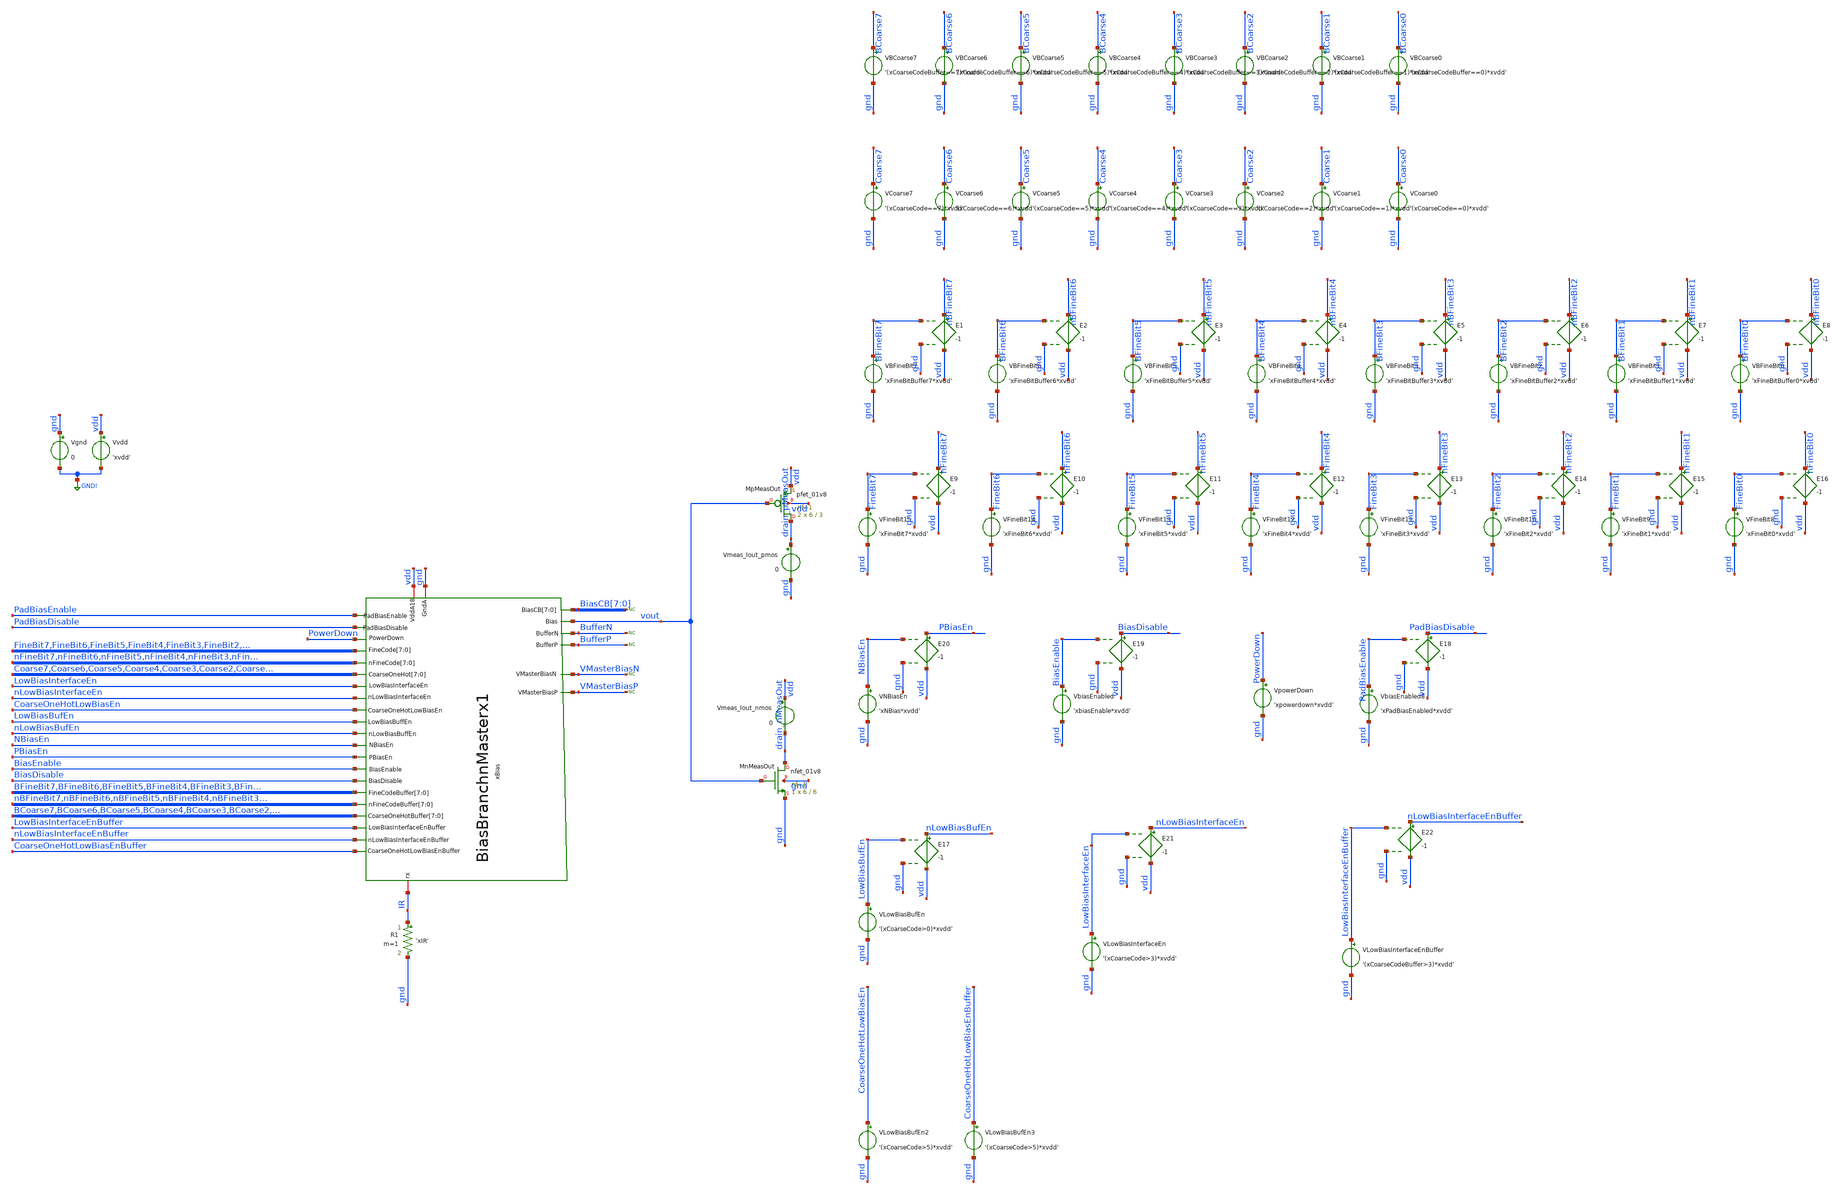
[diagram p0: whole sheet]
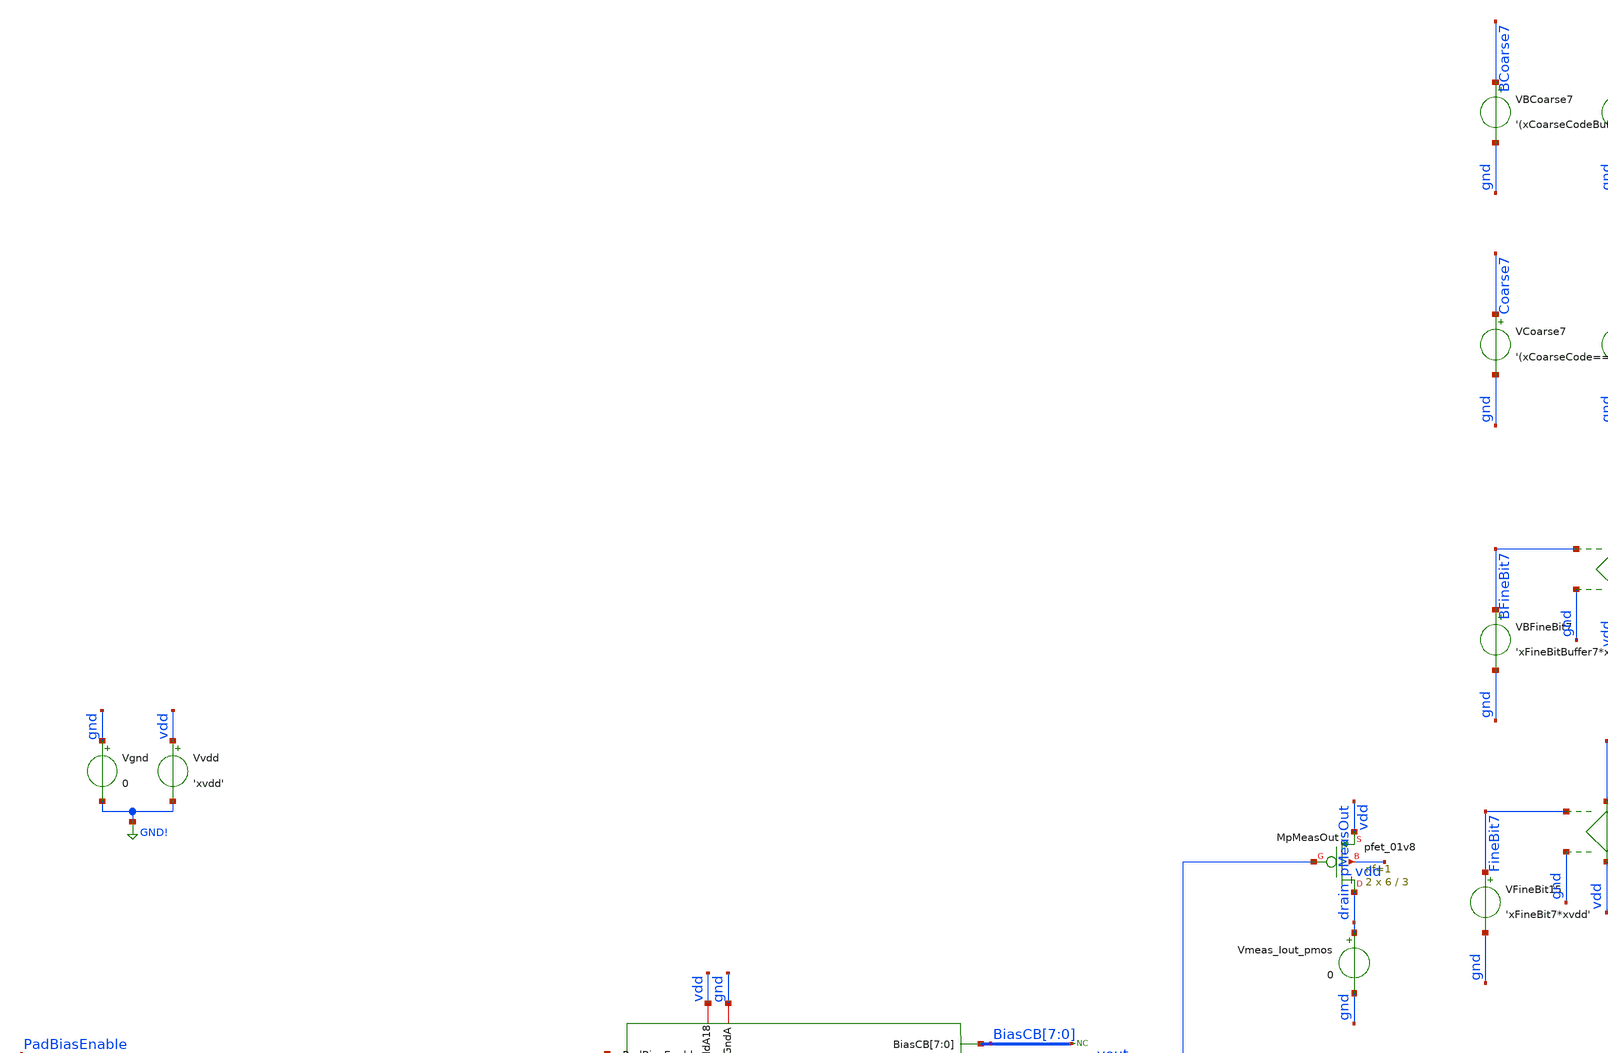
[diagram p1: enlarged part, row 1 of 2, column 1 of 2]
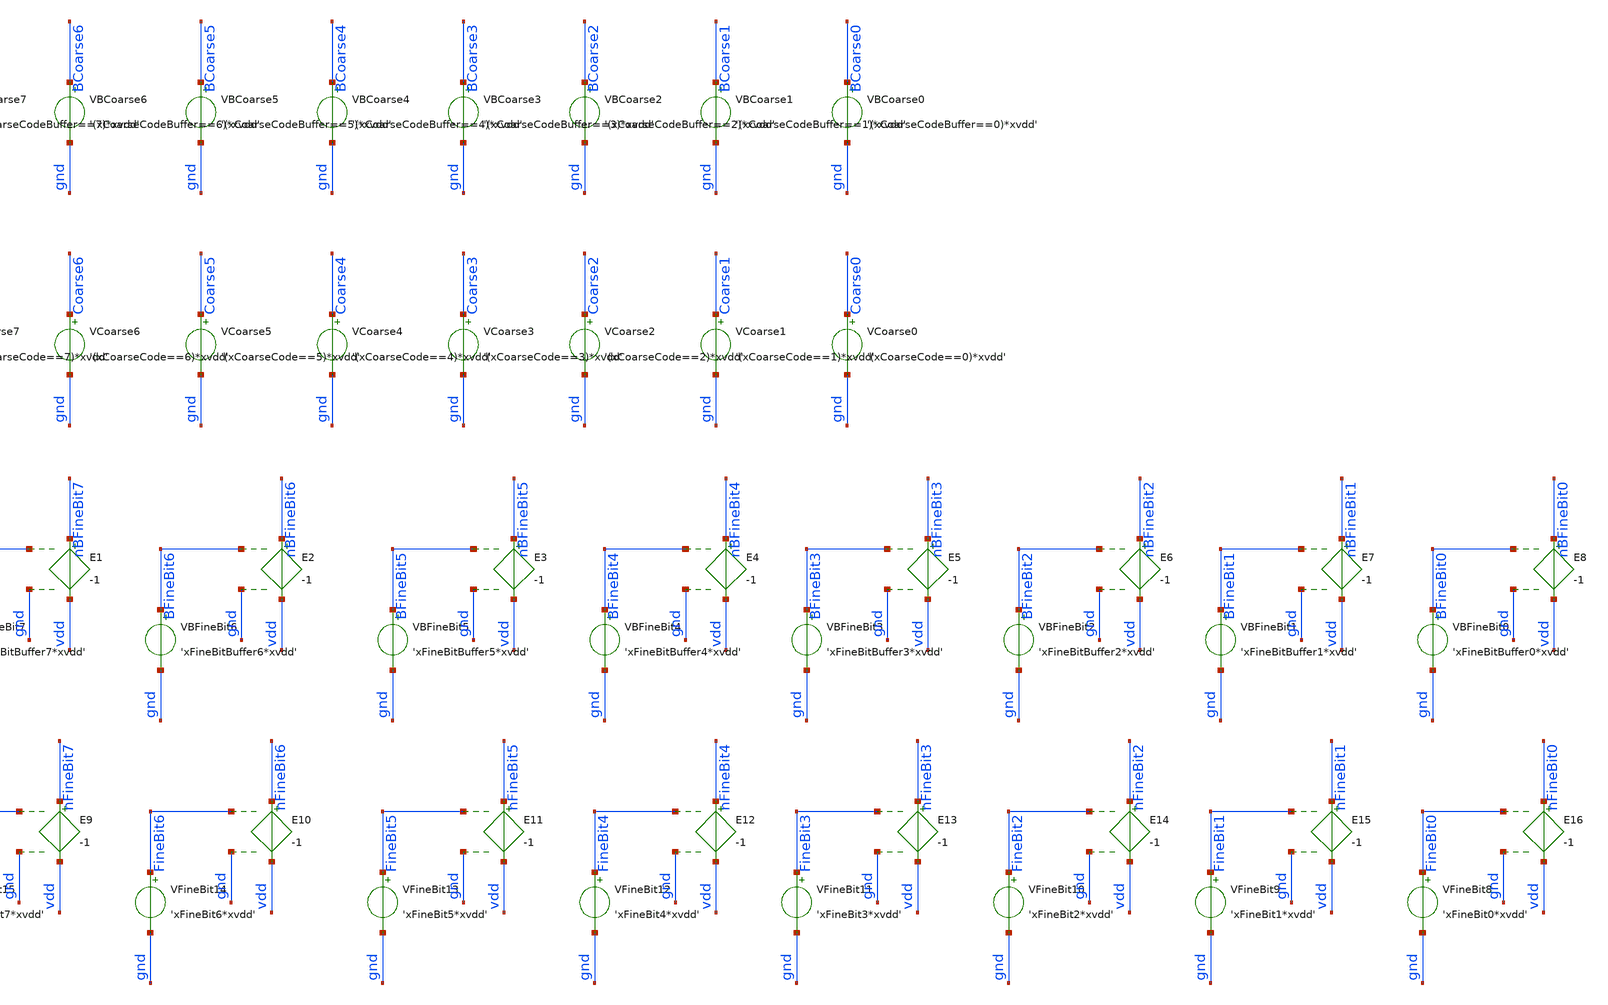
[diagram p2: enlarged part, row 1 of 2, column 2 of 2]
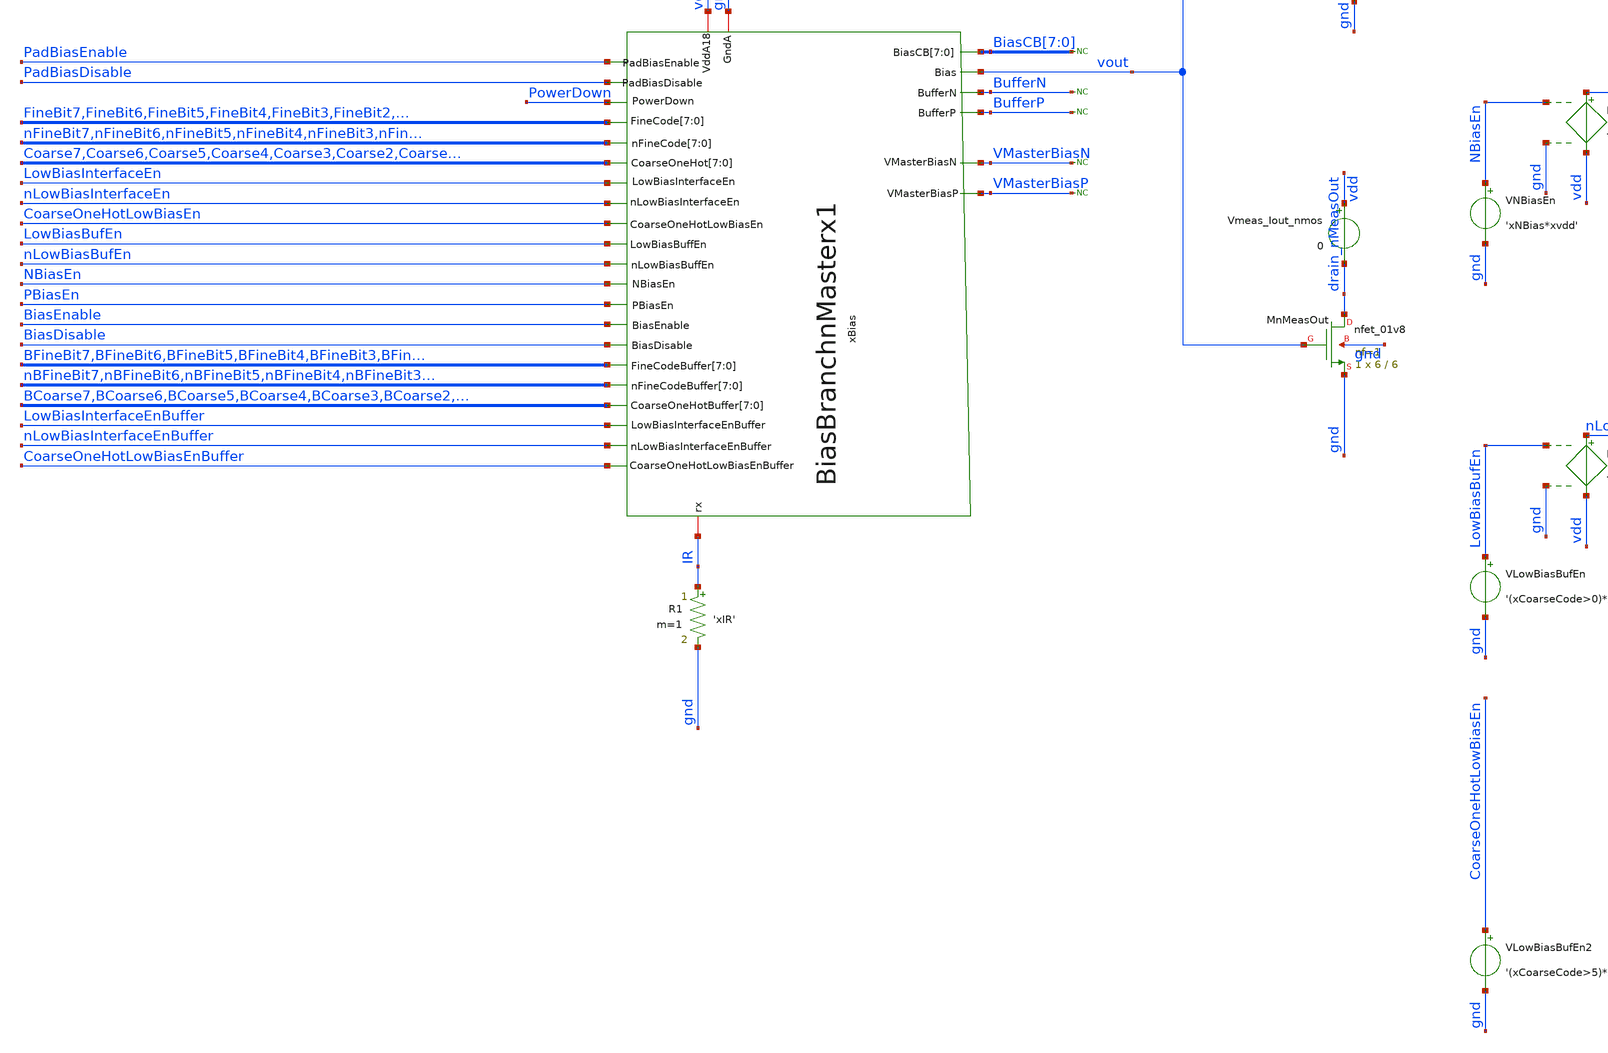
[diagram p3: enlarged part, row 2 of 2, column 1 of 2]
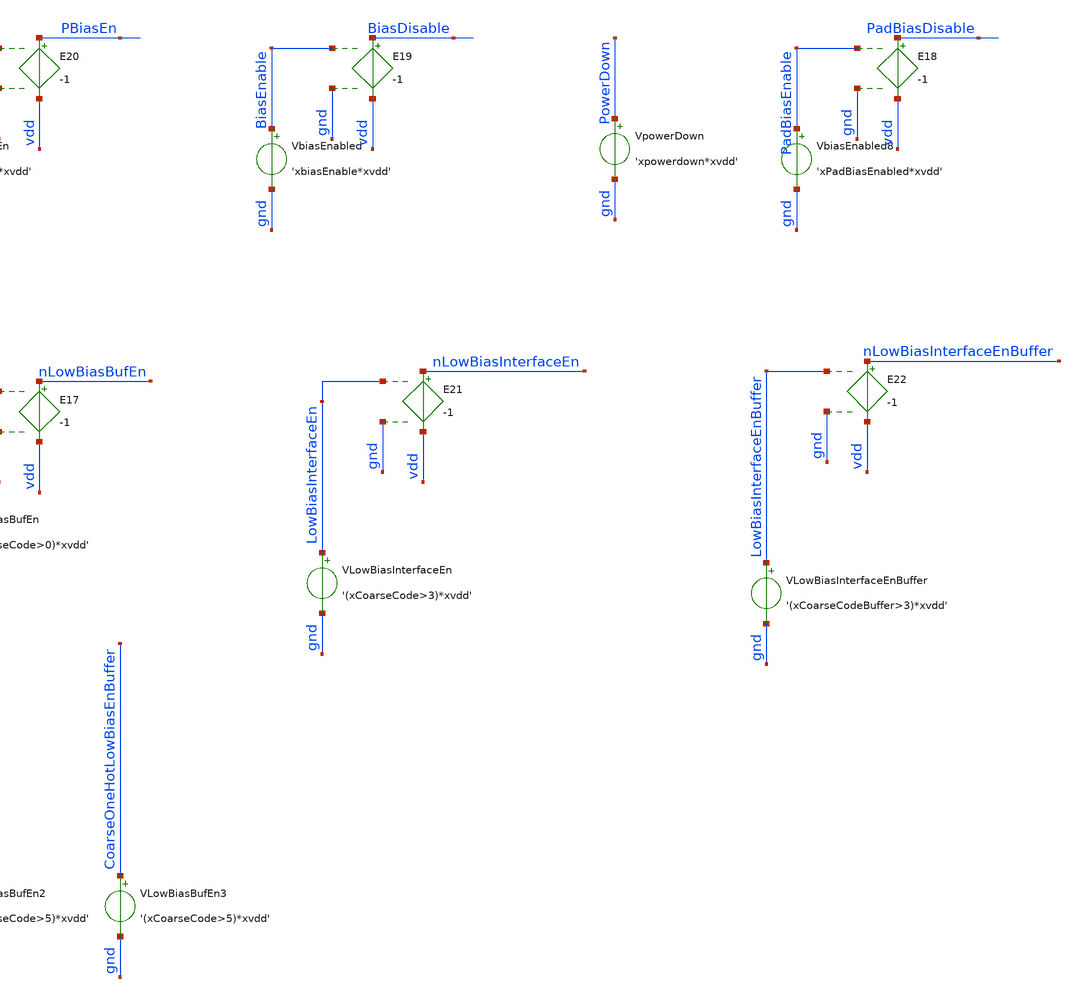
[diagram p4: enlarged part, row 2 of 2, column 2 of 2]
** sch_path: analog/xschem/tb_BiasBranchnMasterx1_op.sch
**.subckt tb_BiasBranchnMasterx1_op
Vgnd gnd GND! 0
.save i(vgnd)
Vvdd vdd GND! 'xvdd'
.save i(vvdd)
VpowerDown PowerDown gnd 'xpowerdown*xvdd'
.save i(vpowerdown)
XMnMeasOut drain_nMeasOut vout gnd gnd sky130_fd_pr__nfet_01v8 L=6 W=6 nf=1 ad='int((1 + 1)/2) * 6 / 1 * 0.29'
+ as='int((1 + 2)/2) * 6 / 1 * 0.29' pd='2*int((1 + 1)/2) * (6 / 1 + 0.29)' ps='2*int((1 + 2)/2) * (6 / 1 + 0.29)'
+ nrd='0.29 / 6 ' nrs='0.29 / 6 ' sa=0 sb=0 sd=0 mult=1 m=1
Vmeas_Iout_nmos vdd drain_nMeasOut 0
.save i(vmeas_iout_nmos)
XMpMeasOut drain_pMeasOut vout vdd vdd sky130_fd_pr__pfet_01v8 L=3 W=6 nf=1 ad='int((1 + 1)/2) * 6 / 1 * 0.29'
+ as='int((1 + 2)/2) * 6 / 1 * 0.29' pd='2*int((1 + 1)/2) * (6 / 1 + 0.29)' ps='2*int((1 + 2)/2) * (6 / 1 + 0.29)'
+ nrd='0.29 / 6 ' nrs='0.29 / 6 ' sa=0 sb=0 sd=0 mult=2 m=2
Vmeas_Iout_pmos drain_pMeasOut gnd 0
.save i(vmeas_iout_pmos)
VbiasEnabled BiasEnable gnd 'xbiasEnable*xvdd'
VNBiasEn NBiasEn gnd 'xNBias*xvdd'
xBias vdd gnd PowerDown BiasCB[7] BiasCB[6] BiasCB[5] BiasCB[4] BiasCB[3] BiasCB[2] BiasCB[1]
+ BiasCB[0] BufferN BufferP VMasterBiasN VMasterBiasP vout IR Coarse7 Coarse6 Coarse5 Coarse4 Coarse3 Coarse2
+ Coarse1 Coarse0 LowBiasInterfaceEn nLowBiasInterfaceEn FineBit7 FineBit6 FineBit5 FineBit4 FineBit3
+ FineBit2 FineBit1 FineBit0 nFineBit7 nFineBit6 nFineBit5 nFineBit4 nFineBit3 nFineBit2 nFineBit1 nFineBit0
+ CoarseOneHotLowBiasEn LowBiasBufEn nLowBiasBufEn NBiasEn PBiasEn BiasEnable BiasDisable BCoarse7 BCoarse6 BCoarse5
+ BCoarse4 BCoarse3 BCoarse2 BCoarse1 BCoarse0 LowBiasInterfaceEnBuffer nLowBiasInterfaceEnBuffer BFineBit7
+ BFineBit6 BFineBit5 BFineBit4 BFineBit3 BFineBit2 BFineBit1 BFineBit0 nBFineBit7 nBFineBit6 nBFineBit5
+ nBFineBit4 nBFineBit3 nBFineBit2 nBFineBit1 nBFineBit0 CoarseOneHotLowBiasEnBuffer PadBiasEnable
+ PadBiasDisable BiasBranchnMasterx1
* noconn BiasCB[7:0]
* noconn BufferN
* noconn BufferP
* noconn VMasterBiasN
* noconn VMasterBiasP
R1 IR gnd 'xIR' m=1
VBFineBit0 BFineBit0 gnd 'xFineBitBuffer0*xvdd'
.save i(vbfinebit0)
VBFineBit1 BFineBit1 gnd 'xFineBitBuffer1*xvdd'
.save i(vbfinebit1)
VBFineBit2 BFineBit2 gnd 'xFineBitBuffer2*xvdd'
.save i(vbfinebit2)
VBFineBit3 BFineBit3 gnd 'xFineBitBuffer3*xvdd'
.save i(vbfinebit3)
VBFineBit4 BFineBit4 gnd 'xFineBitBuffer4*xvdd'
.save i(vbfinebit4)
VBFineBit5 BFineBit5 gnd 'xFineBitBuffer5*xvdd'
.save i(vbfinebit5)
VBFineBit6 BFineBit6 gnd 'xFineBitBuffer6*xvdd'
.save i(vbfinebit6)
VBFineBit7 BFineBit7 gnd 'xFineBitBuffer7*xvdd'
.save i(vbfinebit7)
E1 nBFineBit7 vdd BFineBit7 gnd -1
E2 nBFineBit6 vdd BFineBit6 gnd -1
E3 nBFineBit5 vdd BFineBit5 gnd -1
E4 nBFineBit4 vdd BFineBit4 gnd -1
E5 nBFineBit3 vdd BFineBit3 gnd -1
E6 nBFineBit2 vdd BFineBit2 gnd -1
E7 nBFineBit1 vdd BFineBit1 gnd -1
E8 nBFineBit0 vdd BFineBit0 gnd -1
VFineBit8 FineBit0 gnd 'xFineBit0*xvdd'
.save i(vfinebit8)
VFineBit9 FineBit1 gnd 'xFineBit1*xvdd'
.save i(vfinebit9)
VFineBit10 FineBit2 gnd 'xFineBit2*xvdd'
.save i(vfinebit10)
VFineBit11 FineBit3 gnd 'xFineBit3*xvdd'
.save i(vfinebit11)
VFineBit12 FineBit4 gnd 'xFineBit4*xvdd'
.save i(vfinebit12)
VFineBit13 FineBit5 gnd 'xFineBit5*xvdd'
.save i(vfinebit13)
VFineBit14 FineBit6 gnd 'xFineBit6*xvdd'
.save i(vfinebit14)
VFineBit15 FineBit7 gnd 'xFineBit7*xvdd'
.save i(vfinebit15)
E9 nFineBit7 vdd FineBit7 gnd -1
E10 nFineBit6 vdd FineBit6 gnd -1
E11 nFineBit5 vdd FineBit5 gnd -1
E12 nFineBit4 vdd FineBit4 gnd -1
E13 nFineBit3 vdd FineBit3 gnd -1
E14 nFineBit2 vdd FineBit2 gnd -1
E15 nFineBit1 vdd FineBit1 gnd -1
E16 nFineBit0 vdd FineBit0 gnd -1
VCoarse7 Coarse7 gnd '(xCoarseCode==7)*xvdd'
.save i(vcoarse7)
VCoarse6 Coarse6 gnd '(xCoarseCode==6)*xvdd'
.save i(vcoarse6)
VCoarse5 Coarse5 gnd '(xCoarseCode==5)*xvdd'
.save i(vcoarse5)
VCoarse4 Coarse4 gnd '(xCoarseCode==4)*xvdd'
.save i(vcoarse4)
VCoarse3 Coarse3 gnd '(xCoarseCode==3)*xvdd'
.save i(vcoarse3)
VCoarse2 Coarse2 gnd '(xCoarseCode==2)*xvdd'
.save i(vcoarse2)
VCoarse1 Coarse1 gnd '(xCoarseCode==1)*xvdd'
.save i(vcoarse1)
VCoarse0 Coarse0 gnd '(xCoarseCode==0)*xvdd'
.save i(vcoarse0)
VBCoarse7 BCoarse7 gnd '(xCoarseCodeBuffer==7)*xvdd'
.save i(vbcoarse7)
VBCoarse6 BCoarse6 gnd '(xCoarseCodeBuffer==6)*xvdd'
.save i(vbcoarse6)
VBCoarse5 BCoarse5 gnd '(xCoarseCodeBuffer==5)*xvdd'
.save i(vbcoarse5)
VBCoarse4 BCoarse4 gnd '(xCoarseCodeBuffer==4)*xvdd'
.save i(vbcoarse4)
VBCoarse3 BCoarse3 gnd '(xCoarseCodeBuffer==3)*xvdd'
.save i(vbcoarse3)
VBCoarse2 BCoarse2 gnd '(xCoarseCodeBuffer==2)*xvdd'
.save i(vbcoarse2)
VBCoarse1 BCoarse1 gnd '(xCoarseCodeBuffer==1)*xvdd'
.save i(vbcoarse1)
VBCoarse0 BCoarse0 gnd '(xCoarseCodeBuffer==0)*xvdd'
.save i(vbcoarse0)
VLowBiasBufEn LowBiasBufEn gnd '(xCoarseCode>0)*xvdd'
E17 nLowBiasBufEn vdd LowBiasBufEn gnd -1
E19 BiasDisable vdd BiasEnable gnd -1
E20 PBiasEn vdd NBiasEn gnd -1
VLowBiasInterfaceEn LowBiasInterfaceEn gnd '(xCoarseCode>3)*xvdd'
E21 nLowBiasInterfaceEn vdd LowBiasInterfaceEn gnd -1
VLowBiasInterfaceEnBuffer LowBiasInterfaceEnBuffer gnd '(xCoarseCodeBuffer>3)*xvdd'
E22 nLowBiasInterfaceEnBuffer vdd LowBiasInterfaceEnBuffer gnd -1
VLowBiasBufEn2 CoarseOneHotLowBiasEn gnd '(xCoarseCode>5)*xvdd'
VLowBiasBufEn3 CoarseOneHotLowBiasEnBuffer gnd '(xCoarseCode>5)*xvdd'
VbiasEnabled8 PadBiasEnable gnd 'xPadBiasEnabled*xvdd'
E18 PadBiasDisable vdd PadBiasEnable gnd -1
**** begin user architecture code

** opencircuitdesign pdks install
.lib $::SKYWATER_MODELS/sky130.lib.spice tt




.temp 27

* Flag unsafe operating conditions (exceeds models' specified limits)
.option warn=1

.param xvdd = 1.8
.param xpowerdown = 0
.param xIR = 100k

.param xCoarseCode = 2
.param xFineCode = 71
.param xCoarseCodeBuffer = 1
.param xFineCodeBuffer = 110

.param xPadBiasEnabled = 1
.param xBiasEnable = 1
.param xNBias = 0

.param xCoarseBit0 = (xCoarseCode%2 >= 1)?1:0
.param xCoarseBit1 = ((xCoarseCode/2)%2 >= 1)?1:0
.param xCoarseBit2 = ((xCoarseCode/4)%2 >= 1)?1:0
.param xFineBit0 = (xFineCode%2 >= 1)?1:0
.param xFineBit1 = ((xFineCode/2)%2 >= 1)?1:0
.param xFineBit2 = ((xFineCode/4)%2 >= 1)?1:0
.param xFineBit3 = ((xFineCode/8)%2 >= 1)?1:0
.param xFineBit4 = ((xFineCode/16)%2 >= 1)?1:0
.param xFineBit5 = ((xFineCode/32)%2 >= 1)?1:0
.param xFineBit6 = ((xFineCode/64)%2 >= 1)?1:0
.param xFineBit7 = ((xFineCode/128)%2 >= 1)?1:0

.param xCoarseBitBuffer0 = (xCoarseCodeBuffer%2 >= 1)?1:0
.param xCoarseBitBuffer1 = ((xCoarseCodeBuffer/2)%2 >= 1)?1:0
.param xCoarseBitBuffer2 = ((xCoarseCodeBuffer/4)%2 >= 1)?1:0
.param xFineBitBuffer0 = (xFineCodeBuffer%2 >= 1)?1:0
.param xFineBitBuffer1 = ((xFineCodeBuffer/2)%2 >= 1)?1:0
.param xFineBitBuffer2 = ((xFineCodeBuffer/4)%2 >= 1)?1:0
.param xFineBitBuffer3 = ((xFineCodeBuffer/8)%2 >= 1)?1:0
.param xFineBitBuffer4 = ((xFineCodeBuffer/16)%2 >= 1)?1:0
.param xFineBitBuffer5 = ((xFineCodeBuffer/32)%2 >= 1)?1:0
.param xFineBitBuffer6 = ((xFineCodeBuffer/64)%2 >= 1)?1:0
.param xFineBitBuffer7 = ((xFineCodeBuffer/128)%2 >= 1)?1:0

*.nodeset v(xBias.xBiasBuffer.bit14) = 'xCoarseBitBuffer0*xvdd'
*.nodeset v(xBias.xBiasBuffer.bit13) = 'xCoarseBitBuffer1*xvdd'
*.nodeset v(xBias.xBiasBuffer.bit12) = 'xCoarseBitBuffer0*xvdd'
*.nodeset v(xBias.xBiasBuffer.xDivFine.Q7) = 'xFineBitBuffer7*xvdd'
*.nodeset v(xBias.xBiasBuffer.xDivFine.Q6) = 'xFineBitBuffer6*xvdd'
*.nodeset v(xBias.xBiasBuffer.xDivFine.Q5) = 'xFineBitBuffer5*xvdd'
*.nodeset v(xBias.xBiasBuffer.xDivFine.Q4) = 'xFineBitBuffer4*xvdd'
*.nodeset v(xBias.xBiasBuffer.xDivFine.Q3) = 'xFineBitBuffer3*xvdd'
*.nodeset v(xBias.xBiasBuffer.xDivFine.Q2) = 'xFineBitBuffer2*xvdd'
*.nodeset v(xBias.xBiasBuffer.xDivFine.Q1) = 'xFineBitBuffer1*xvdd'
*.nodeset v(xBias.xBiasBuffer.xDivFine.Q0) = 'xFineBitBuffer0*xvdd'



.save v(@m.xBias.xBiasMasternCoarse.xBiasMasterBias.xMNBias.msky130_fd_pr__nfet_01v8_lvt[vdsat])
.save @m.xBias.xBiasMasternCoarse.xBiasMasterBias.xMNBias.msky130_fd_pr__nfet_01v8_lvt[id]
.save v(@m.xBias.xBiasMasternCoarse.xBiasMasterBias.xMNBiasDio.msky130_fd_pr__nfet_01v8_lvt[vdsat])
.save @m.xBias.xBiasMasternCoarse.xBiasMasterBias.xMNBiasDio.msky130_fd_pr__nfet_01v8_lvt[id]
.save v(@m.xBias.xBiasMasternCoarse.xBiasMasterBias.xMNBiasCascDio.msky130_fd_pr__nfet_01v8_lvt[vdsat])
.save v(@m.xBias.xBiasMasternCoarse.xBiasMasterBias.xMNBiasCasc.msky130_fd_pr__nfet_01v8_lvt[vdsat])
.save v(@m.xBias.xBiasMasternCoarse.xBiasMasterBias.xMPBias.msky130_fd_pr__pfet_01v8_lvt[vdsat])
.save v(@m.xBias.xBiasMasternCoarse.xBiasMasterBias.xMPBiasDio.msky130_fd_pr__pfet_01v8_lvt[vdsat])
.save v(@m.xBias.xBiasMasternCoarse.xBiasMasterBias.xMNMirr1.msky130_fd_pr__nfet_01v8_lvt[vdsat])
.save @m.xBias.xBiasMasternCoarse.xBiasMasterBias.xMNMirr1.msky130_fd_pr__nfet_01v8_lvt[id]
.save v(@m.xBias.xBiasMasternCoarse.xBiasMasterBias.xMNMirr2.msky130_fd_pr__nfet_01v8_lvt[vdsat])
.save @m.xBias.xBiasMasternCoarse.xBiasMasterBias.xMNMirr2.msky130_fd_pr__nfet_01v8_lvt[id]
.save v(@m.xBias.xBiasMasternCoarse.xBiasMasterBias.xMNMirrCasc1.msky130_fd_pr__nfet_01v8_lvt[vdsat])
.save v(@m.xBias.xBiasMasternCoarse.xBiasMasterBias.xMNMirrCasc2.msky130_fd_pr__nfet_01v8_lvt[vdsat])
.save @m.xBias.xBiasMasternCoarse.xMBDiv.xMNDioCB0.msky130_fd_pr__nfet_01v8_lvt[id]
.save @m.xBias.xBiasMasternCoarse.xMBDiv.xMNDioCB1.msky130_fd_pr__nfet_01v8_lvt[id]
.save @m.xBias.xBiasMasternCoarse.xMBDiv.xMNDioCB2.msky130_fd_pr__nfet_01v8_lvt[id]
.save @m.xBias.xBiasMasternCoarse.xMBDiv.xMNDioCB3.msky130_fd_pr__nfet_01v8_lvt[id]
.save @m.xBias.xBiasMasternCoarse.xMBDiv.xMNDioCB4.msky130_fd_pr__nfet_01v8_lvt[id]
.save @m.xBias.xBiasMasternCoarse.xMBDiv.xMNDioCB5.msky130_fd_pr__nfet_01v8_lvt[id]
.save @m.xBias.xBiasMasternCoarse.xMBDiv.xMNDioCB6.msky130_fd_pr__nfet_01v8_lvt[id]
.save @m.xBias.xBiasMasternCoarse.xMBDiv.xMNDioCB7.msky130_fd_pr__nfet_01v8_lvt[id]
.save @m.xBias.xBiasBranch.xCoarseBuf.xSel.xMmirrB0.msky130_fd_pr__nfet_01v8_lvt[id]
.save @m.xBias.xBiasBranch.xCoarseBuf.xSel.xMmirrB1.msky130_fd_pr__nfet_01v8_lvt[id]
.save @m.xBias.xBiasBranch.xCoarseBuf.xSel.xMmirrhB2.msky130_fd_pr__nfet_01v8_lvt[id]
.save @m.xBias.xBiasBranch.xCoarseBuf.xSel.xMmirrhB3.msky130_fd_pr__nfet_01v8_lvt[id]
.save @m.xBias.xBiasBranch.xCoarseBuf.xSel.xMmirrhB4t07.msky130_fd_pr__nfet_01v8_lvt[id]
.save v(@m.xBias.xBiasBranch.xCoarseBuf.xSel.xMmirrB0.msky130_fd_pr__nfet_01v8_lvt[vdsat])
.save v(@m.xBias.xBiasBranch.xCoarseBuf.xSel.xMmirrB1.msky130_fd_pr__nfet_01v8_lvt[vdsat])
.save v(@m.xBias.xBiasBranch.xCoarseBuf.xSel.xMmirrhB2.msky130_fd_pr__nfet_01v8_lvt[vdsat])
.save v(@m.xBias.xBiasBranch.xCoarseBuf.xSel.xMmirrhB3.msky130_fd_pr__nfet_01v8_lvt[vdsat])
.save v(@m.xBias.xBiasBranch.xCoarseBuf.xSel.xMmirrhB4t07.msky130_fd_pr__nfet_01v8_lvt[vdsat])
.save @m.xBias.xBiasBranch.xCoarse2Fine.xMpDioOut.msky130_fd_pr__pfet_01v8_lvt[id]
.save @m.xBias.xBiasBranch.xCoarse2Fine.xMpMirrOut.msky130_fd_pr__pfet_01v8_lvt[id]
.save @m.xBias.xBiasBranch.xCoarse2Fine.xMpDionOut2.msky130_fd_pr__pfet_01v8_lvt[id]
.save @m.xBias.xBiasBranch.xCoarse2Fine.xMpMirrnOut2.msky130_fd_pr__pfet_01v8_lvt[id]
.save v(@m.xBias.xBiasBranch.xCoarse2Fine.xMpDioOut.msky130_fd_pr__pfet_01v8_lvt[vdsat])
.save v(@m.xBias.xBiasBranch.xCoarse2Fine.xMpMirrOut.msky130_fd_pr__pfet_01v8_lvt[vdsat])
.save v(@m.xBias.xBiasBranch.xCoarse2Fine.xMpDionOut2.msky130_fd_pr__pfet_01v8_lvt[vdsat])
.save v(@m.xBias.xBiasBranch.xCoarse2Fine.xMpMirrnOut2.msky130_fd_pr__pfet_01v8_lvt[vdsat])
.save @m.xBias.xBiasBranch.xCoarse2Fine.xMpInDio.msky130_fd_pr__pfet_01v8_lvt[id]
.save @m.xBias.xBiasBranch.xBuffs.xMnDio.msky130_fd_pr__nfet_01v8[id]
.save @m.xBias.xBiasBranch.xBuffs.xMnMirr.msky130_fd_pr__nfet_01v8[id]
.save @m.xBias.xBiasBranch.xBuffs.xMnMirrBuffBias.msky130_fd_pr__nfet_01v8_lvt[id]
.save @m.xBias.xBiasBranch.xBuffs.xMnMirrBuffB0.msky130_fd_pr__nfet_01v8_lvt[id]
.save @m.xBias.xBiasBranch.xBuffs.xMnMirrBuffnB0.msky130_fd_pr__nfet_01v8_lvt[id]
.save v(@m.xBias.xBiasBranch.xBuffs.xMnDio.msky130_fd_pr__nfet_01v8[vdsat])
.save v(@m.xBias.xBiasBranch.xBuffs.xMnMirr.msky130_fd_pr__nfet_01v8[vdsat])
.save v(@m.xBias.xBiasBranch.xBuffs.xMnMirrBuffBias.msky130_fd_pr__nfet_01v8_lvt[vdsat])
.save v(@m.xBias.xBiasBranch.xBuffs.xMnMirrBuffB0.msky130_fd_pr__nfet_01v8_lvt[vdsat])
.save v(@m.xBias.xBiasBranch.xBuffs.xMnMirrBuffnB0.msky130_fd_pr__nfet_01v8_lvt[vdsat])
.save @m.xBias.xBiasBranch.xBuffs.xMpDio.msky130_fd_pr__pfet_01v8[id]
.save @m.xBias.xBiasBranch.xBuffs.xMpMirrBuffBias.msky130_fd_pr__pfet_01v8_lvt[id]
.save @m.xBias.xBiasBranch.xBuffs.xMpMirrBuffB0.msky130_fd_pr__pfet_01v8_lvt[id]
.save @m.xBias.xBiasBranch.xBuffs.xMpMirrBuffnB0.msky130_fd_pr__pfet_01v8_lvt[id]
.save v(@m.xBias.xBiasBranch.xBuffs.xMpDio.msky130_fd_pr__pfet_01v8[vdsat])
.save v(@m.xBias.xBiasBranch.xBuffs.xMpMirrBuffBias.msky130_fd_pr__pfet_01v8_lvt[vdsat])
.save v(@m.xBias.xBiasBranch.xBuffs.xMpMirrBuffB0.msky130_fd_pr__pfet_01v8_lvt[vdsat])
.save v(@m.xBias.xBiasBranch.xBuffs.xMpMirrBuffnB0.msky130_fd_pr__pfet_01v8_lvt[vdsat])
.save @m.xBias.xBiasBuffer.xCoarseBuf.xSel.xMmirrB0.msky130_fd_pr__nfet_01v8_lvt[id]
.save @m.xBias.xBiasBuffer.xCoarseBuf.xSel.xMmirrB1.msky130_fd_pr__nfet_01v8_lvt[id]
.save @m.xBias.xBiasBuffer.xCoarseBuf.xSel.xMmirrhB2.msky130_fd_pr__nfet_01v8_lvt[id]
.save @m.xBias.xBiasBuffer.xCoarseBuf.xSel.xMmirrhB3.msky130_fd_pr__nfet_01v8_lvt[id]
.save @m.xBias.xBiasBuffer.xCoarseBuf.xSel.xMmirrhB4t07.msky130_fd_pr__nfet_01v8_lvt[id]
.save v(@m.xBias.xBiasBuffer.xCoarseBuf.xSel.xMmirrB0.msky130_fd_pr__nfet_01v8_lvt[vdsat])
.save v(@m.xBias.xBiasBuffer.xCoarseBuf.xSel.xMmirrB1.msky130_fd_pr__nfet_01v8_lvt[vdsat])
.save v(@m.xBias.xBiasBuffer.xCoarseBuf.xSel.xMmirrhB2.msky130_fd_pr__nfet_01v8_lvt[vdsat])
.save v(@m.xBias.xBiasBuffer.xCoarseBuf.xSel.xMmirrhB3.msky130_fd_pr__nfet_01v8_lvt[vdsat])
.save v(@m.xBias.xBiasBuffer.xCoarseBuf.xSel.xMmirrhB4t07.msky130_fd_pr__nfet_01v8_lvt[vdsat])
.save @m.xBias.xBiasBuffer.xCoarse2Fine.xMpDioOut.msky130_fd_pr__pfet_01v8_lvt[id]
.save @m.xBias.xBiasBuffer.xCoarse2Fine.xMpMirrOut.msky130_fd_pr__pfet_01v8_lvt[id]
.save @m.xBias.xBiasBuffer.xCoarse2Fine.xMpDionOut2.msky130_fd_pr__pfet_01v8_lvt[id]
.save @m.xBias.xBiasBuffer.xCoarse2Fine.xMpMirrnOut2.msky130_fd_pr__pfet_01v8_lvt[id]
.save v(@m.xBias.xBiasBuffer.xCoarse2Fine.xMpDioOut.msky130_fd_pr__pfet_01v8_lvt[vdsat])
.save v(@m.xBias.xBiasBuffer.xCoarse2Fine.xMpMirrOut.msky130_fd_pr__pfet_01v8_lvt[vdsat])
.save v(@m.xBias.xBiasBuffer.xCoarse2Fine.xMpDionOut2.msky130_fd_pr__pfet_01v8_lvt[vdsat])
.save v(@m.xBias.xBiasBuffer.xCoarse2Fine.xMpMirrnOut2.msky130_fd_pr__pfet_01v8_lvt[vdsat])
.save @m.xBias.xBiasBuffer.xCoarse2Fine.xMpInDio.msky130_fd_pr__pfet_01v8_lvt[id]
.save @m.xBias.xBiasBuffer.xMnDio.msky130_fd_pr__nfet_01v8_lvt[id]
.save @m.xBias.xBiasBuffer.xMnMirr.msky130_fd_pr__nfet_01v8_lvt[id]
.save @m.xBias.xBiasBuffer.xMpDio.msky130_fd_pr__pfet_01v8_lvt[id]
.save v(@m.xBias.xBiasBuffer.xMnDio.msky130_fd_pr__nfet_01v8_lvt[vdsat])
.save v(@m.xBias.xBiasBuffer.xMnMirr.msky130_fd_pr__nfet_01v8_lvt[vdsat])
.save v(@m.xBias.xBiasBuffer.xMpDio.msky130_fd_pr__pfet_01v8_lvt[vdsat])


.save all

.op


**** end user architecture code
**.ends
.GLOBAL GND!
.end
